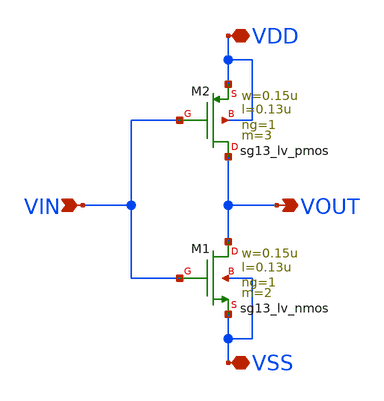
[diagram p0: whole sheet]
** sch_path: Custom_std_cells/inv.sch
**.subckt inv VDD VSS VOUT VIN
*.iopin VDD
*.iopin VSS
*.opin VOUT
*.ipin VIN
XM2 VOUT VIN VDD VDD sg13_lv_pmos w=0.15u l=0.13u ng=1 m=3 mm_ok=1
XM1 VOUT VIN VSS VSS sg13_lv_nmos w=0.15u l=0.13u ng=1 m=2 mm_ok=1
**.ends
.end
